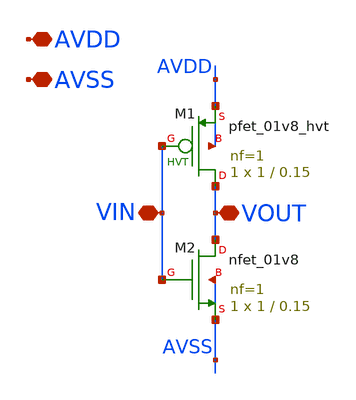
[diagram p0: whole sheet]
** sch_path: xschem/inv_test.sch
**.subckt inv_test AVDD AVSS VIN VOUT
*.iopin AVDD
*.iopin AVSS
*.iopin VIN
*.iopin VOUT
XM1 VOUT VIN AVDD AVDD sky130_fd_pr__pfet_01v8_hvt L=0.15 W=1 nf=1 ad='int((nf+1)/2) * W/nf * 0.29' as='int((nf+2)/2) * W/nf * 0.29'
+ pd='2*int((nf+1)/2) * (W/nf + 0.29)' ps='2*int((nf+2)/2) * (W/nf + 0.29)' nrd='0.29 / W' nrs='0.29 / W'
+ sa=0 sb=0 sd=0 mult=1 m=1
XM2 VOUT VIN AVSS AVSS sky130_fd_pr__nfet_01v8 L=0.15 W=1 nf=1 ad='int((nf+1)/2) * W/nf * 0.29' as='int((nf+2)/2) * W/nf * 0.29'
+ pd='2*int((nf+1)/2) * (W/nf + 0.29)' ps='2*int((nf+2)/2) * (W/nf + 0.29)' nrd='0.29 / W' nrs='0.29 / W'
+ sa=0 sb=0 sd=0 mult=1 m=1
**.ends
.end
